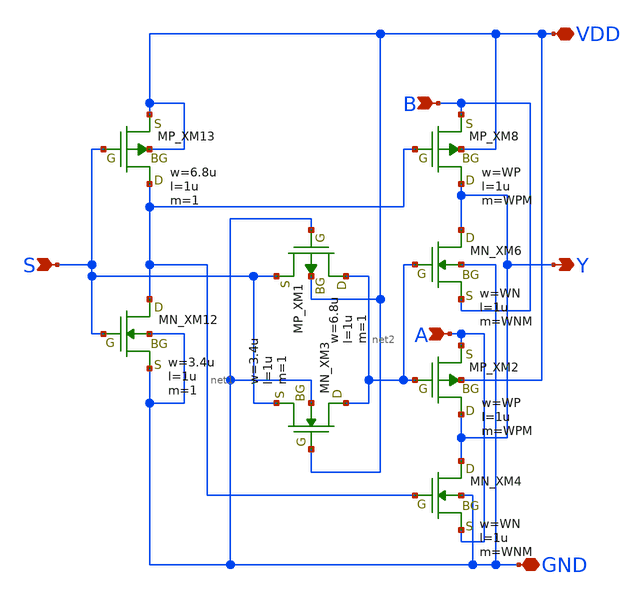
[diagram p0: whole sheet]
** sch_path: Vol.2/files/05/xschem/AMUX2.sch
**.subckt AMUX2 B S Y VDD GND A
*.ipin B
*.ipin S
*.opin Y
*.iopin VDD
*.iopin GND
*.ipin A
XM13 net1 S VDD VDD PMOS w=6.8u l=1u as=0 ad=0 ps=0 pd=0 nrd=0 nrs=0 m=1
XM8 Y net1 B VDD PMOS w=WP l=1u as=0 ad=0 ps=0 pd=0 nrd=0 nrs=0 m=WPM
XM2 Y net2 A VDD PMOS w=WP l=1u as=0 ad=0 ps=0 pd=0 nrd=0 nrs=0 m=WPM
XM12 net1 S GND GND NMOS w=3.4u l=1u as=0 ad=0 ps=0 pd=0 nrd=0 nrs=0 m=1
XM6 Y net2 B GND NMOS w=WN l=1u as=0 ad=0 ps=0 pd=0 nrd=0 nrs=0 m=WNM
XM4 Y net1 A GND NMOS w=WN l=1u as=0 ad=0 ps=0 pd=0 nrd=0 nrs=0 m=WNM
XM1 net2 GND S VDD PMOS w=6.8u l=1u as=0 ad=0 ps=0 pd=0 nrd=0 nrs=0 m=1
XM3 net2 VDD S GND NMOS w=3.4u l=1u as=0 ad=0 ps=0 pd=0 nrd=0 nrs=0 m=1
**.ends
.end
